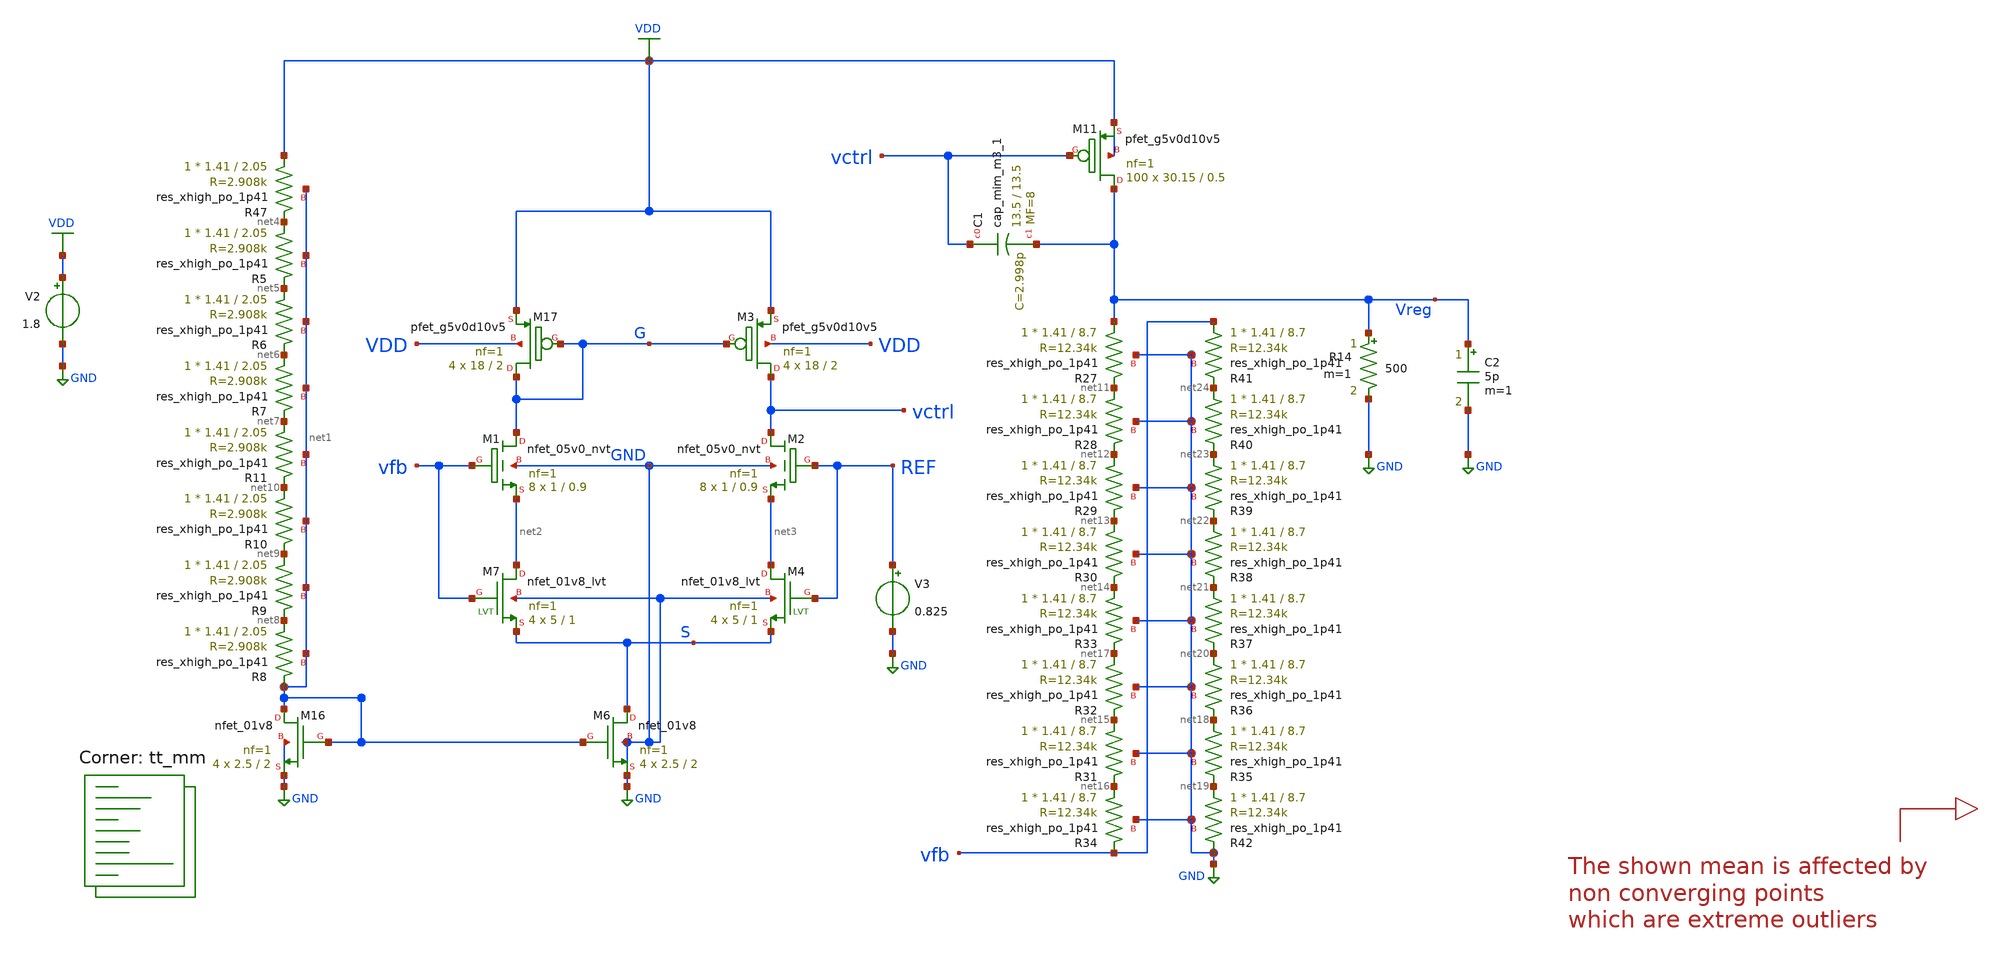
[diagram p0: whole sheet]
** sch_path: ALDO/Testbenches/LDO4_stef_MC.sch
**.subckt LDO4_stef_MC
XM11 Vreg vctrl VDD VDD sky130_fd_pr__pfet_g5v0d10v5 L=0.5 W=30.15 nf=1 ad='int((nf+1)/2) * W/nf * 0.29'
+ as='int((nf+2)/2) * W/nf * 0.29' pd='2*int((nf+1)/2) * (W/nf + 0.29)' ps='2*int((nf+2)/2) * (W/nf + 0.29)'
+ nrd='0.29 / W' nrs='0.29 / W' sa=0 sb=0 sd=0 mult=100 m=100
V3 REF GND 0.825
C2 Vreg GND 5p m=1
XM16 net1 net1 GND GND sky130_fd_pr__nfet_01v8 L=2 W=2.5 nf=1 ad='int((nf+1)/2) * W/nf * 0.29' as='int((nf+2)/2) * W/nf * 0.29'
+ pd='2*int((nf+1)/2) * (W/nf + 0.29)' ps='2*int((nf+2)/2) * (W/nf + 0.29)' nrd='0.29 / W' nrs='0.29 / W'
+ sa=0 sb=0 sd=0 mult=4 m=4
XM3 vctrl G VDD VDD sky130_fd_pr__pfet_g5v0d10v5 L=2 W=18 nf=1 ad='int((nf+1)/2) * W/nf * 0.29' as='int((nf+2)/2) * W/nf * 0.29'
+ pd='2*int((nf+1)/2) * (W/nf + 0.29)' ps='2*int((nf+2)/2) * (W/nf + 0.29)' nrd='0.29 / W' nrs='0.29 / W'
+ sa=0 sb=0 sd=0 mult=4 m=4
XM17 G G VDD VDD sky130_fd_pr__pfet_g5v0d10v5 L=2 W=18 nf=1 ad='int((nf+1)/2) * W/nf * 0.29' as='int((nf+2)/2) * W/nf * 0.29'
+ pd='2*int((nf+1)/2) * (W/nf + 0.29)' ps='2*int((nf+2)/2) * (W/nf + 0.29)' nrd='0.29 / W' nrs='0.29 / W'
+ sa=0 sb=0 sd=0 mult=4 m=4
XR47 VDD net4 net1 sky130_fd_pr__res_xhigh_po_1p41 L=2.05 mult=1 m=1
XR5 net4 net5 net1 sky130_fd_pr__res_xhigh_po_1p41 L=2.05 mult=1 m=1
XR6 net5 net6 net1 sky130_fd_pr__res_xhigh_po_1p41 L=2.05 mult=1 m=1
XR7 net6 net7 net1 sky130_fd_pr__res_xhigh_po_1p41 L=2.05 mult=1 m=1
XR8 net8 net1 net1 sky130_fd_pr__res_xhigh_po_1p41 L=2.05 mult=1 m=1
XR9 net9 net8 net1 sky130_fd_pr__res_xhigh_po_1p41 L=2.05 mult=1 m=1
XR10 net10 net9 net1 sky130_fd_pr__res_xhigh_po_1p41 L=2.05 mult=1 m=1
XR11 net7 net10 net1 sky130_fd_pr__res_xhigh_po_1p41 L=2.05 mult=1 m=1
XR27 Vreg net11 GND sky130_fd_pr__res_xhigh_po_1p41 L=8.7 mult=1 m=1
XR28 net11 net12 GND sky130_fd_pr__res_xhigh_po_1p41 L=8.7 mult=1 m=1
XR29 net12 net13 GND sky130_fd_pr__res_xhigh_po_1p41 L=8.7 mult=1 m=1
XR30 net13 net14 GND sky130_fd_pr__res_xhigh_po_1p41 L=8.7 mult=1 m=1
XR31 net15 net16 GND sky130_fd_pr__res_xhigh_po_1p41 L=8.7 mult=1 m=1
XR32 net17 net15 GND sky130_fd_pr__res_xhigh_po_1p41 L=8.7 mult=1 m=1
XR33 net14 net17 GND sky130_fd_pr__res_xhigh_po_1p41 L=8.7 mult=1 m=1
XR34 net16 vfb GND sky130_fd_pr__res_xhigh_po_1p41 L=8.7 mult=1 m=1
XR35 net18 net19 GND sky130_fd_pr__res_xhigh_po_1p41 L=8.7 mult=1 m=1
XR36 net20 net18 GND sky130_fd_pr__res_xhigh_po_1p41 L=8.7 mult=1 m=1
XR37 net21 net20 GND sky130_fd_pr__res_xhigh_po_1p41 L=8.7 mult=1 m=1
XR38 net22 net21 GND sky130_fd_pr__res_xhigh_po_1p41 L=8.7 mult=1 m=1
XR39 net23 net22 GND sky130_fd_pr__res_xhigh_po_1p41 L=8.7 mult=1 m=1
XR40 net24 net23 GND sky130_fd_pr__res_xhigh_po_1p41 L=8.7 mult=1 m=1
XR41 vfb net24 GND sky130_fd_pr__res_xhigh_po_1p41 L=8.7 mult=1 m=1
XR42 net19 GND GND sky130_fd_pr__res_xhigh_po_1p41 L=8.7 mult=1 m=1
XC1 vctrl Vreg sky130_fd_pr__cap_mim_m3_1 W=13.5 L=13.5 MF=8 m=8
XM6 S net1 GND GND sky130_fd_pr__nfet_01v8 L=2 W=2.5 nf=1 ad='int((nf+1)/2) * W/nf * 0.29' as='int((nf+2)/2) * W/nf * 0.29'
+ pd='2*int((nf+1)/2) * (W/nf + 0.29)' ps='2*int((nf+2)/2) * (W/nf + 0.29)' nrd='0.29 / W' nrs='0.29 / W'
+ sa=0 sb=0 sd=0 mult=4 m=4
XM1 G vfb net2 GND sky130_fd_pr__nfet_05v0_nvt L=0.9 W=1 nf=1 ad='int((nf+1)/2) * W/nf * 0.29' as='int((nf+2)/2) * W/nf * 0.29'
+ pd='2*int((nf+1)/2) * (W/nf + 0.29)' ps='2*int((nf+2)/2) * (W/nf + 0.29)' nrd='0.29 / W' nrs='0.29 / W'
+ sa=0 sb=0 sd=0 mult=8 m=8
XM2 vctrl REF net3 GND sky130_fd_pr__nfet_05v0_nvt L=0.9 W=1 nf=1 ad='int((nf+1)/2) * W/nf * 0.29' as='int((nf+2)/2) * W/nf * 0.29'
+ pd='2*int((nf+1)/2) * (W/nf + 0.29)' ps='2*int((nf+2)/2) * (W/nf + 0.29)' nrd='0.29 / W' nrs='0.29 / W'
+ sa=0 sb=0 sd=0 mult=8 m=8
XM7 net2 vfb S GND sky130_fd_pr__nfet_01v8_lvt L=1 W=5 nf=1 ad='int((nf+1)/2) * W/nf * 0.29' as='int((nf+2)/2) * W/nf * 0.29'
+ pd='2*int((nf+1)/2) * (W/nf + 0.29)' ps='2*int((nf+2)/2) * (W/nf + 0.29)' nrd='0.29 / W' nrs='0.29 / W'
+ sa=0 sb=0 sd=0 mult=4 m=4
XM4 net3 REF S GND sky130_fd_pr__nfet_01v8_lvt L=1 W=5 nf=1 ad='int((nf+1)/2) * W/nf * 0.29' as='int((nf+2)/2) * W/nf * 0.29'
+ pd='2*int((nf+1)/2) * (W/nf + 0.29)' ps='2*int((nf+2)/2) * (W/nf + 0.29)' nrd='0.29 / W' nrs='0.29 / W'
+ sa=0 sb=0 sd=0 mult=4 m=4
V2 VDD GND 1.8
R14 Vreg GND 500 m=1
**** begin user architecture code
.lib $::SKYWATER_MODELS/sky130.lib.spice tt_mm


.options savecurrents itl2=100 method=gear KEEPOPINFO
.control
 let runs=1000
 let r=0
 setseed 23
 dowhile r < runs
   reset
   op
   let run=r
   remzerovec
   write LDO4_stef_MC.raw
   set appendwrite
   print v(Vreg)
   let r = r + 1
 end

.endc


**** end user architecture code
**.ends
.GLOBAL VDD
.GLOBAL GND
.end
